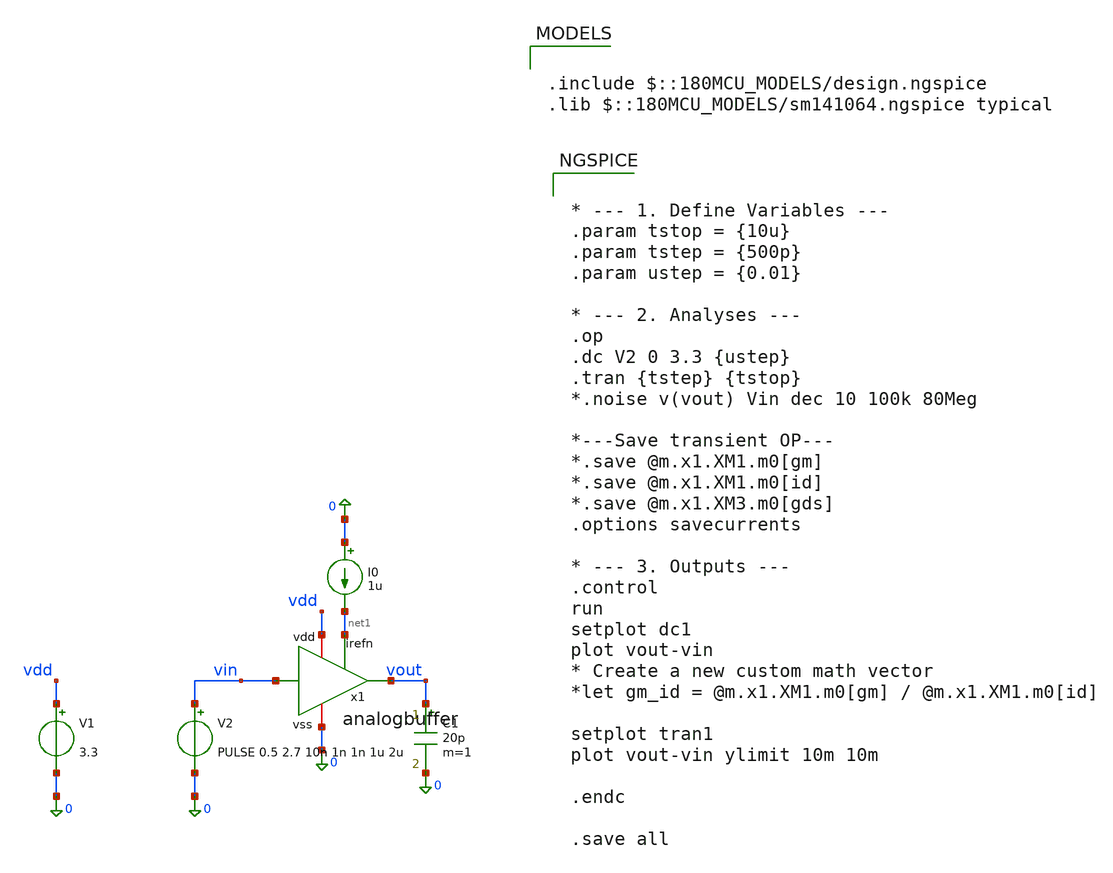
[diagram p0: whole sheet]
** sch_path: Tobias/2026 07 15 Intermediate Results/analogbuffer/analogbuffer-tb.sch
**.subckt analogbuffer-tb
x1 vdd net1 vin vout 0 analogbuffer
I0 0 net1 1u
V1 vdd 0 3.3
V2 vin 0 PULSE 0.5 2.7 10n 1n 1n 1u 2u
C1 vout 0 20p m=1
**** begin user architecture code


* --- 1. Define Variables ---
.param tstop = {10u}
.param tstep = {500p}
.param ustep = {0.01}

* --- 2. Analyses ---
.op
.dc V2 0 3.3 {ustep}
.tran {tstep} {tstop}
*.noise v(vout) Vin dec 10 100k 80Meg

*---Save transient OP---
*.save @m.x1.XM1.m0[gm]
*.save @m.x1.XM1.m0[id]
*.save @m.x1.XM3.m0[gds]
.options savecurrents

* --- 3. Outputs ---
.control
run
setplot dc1
plot vout-vin
* Create a new custom math vector
*let gm_id = @m.x1.XM1.m0[gm] / @m.x1.XM1.m0[id]

setplot tran1
plot vout-vin ylimit 10m 10m

.endc

.save all



.include $::180MCU_MODELS/design.ngspice
.lib $::180MCU_MODELS/sm141064.ngspice typical

**** end user architecture code
**.ends
.end
